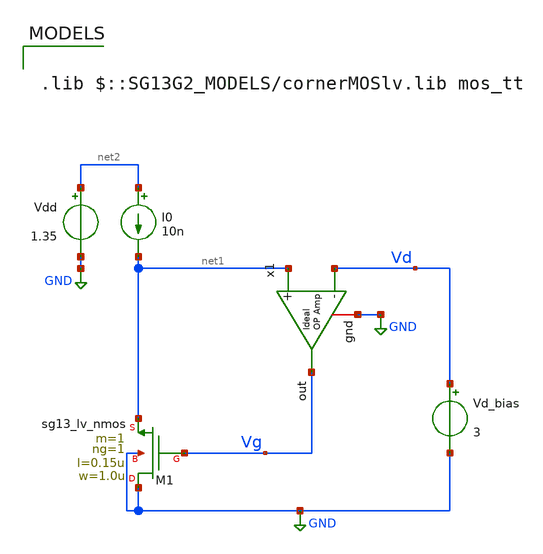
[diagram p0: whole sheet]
** sch_path: ihp_tutorials/nmos_ext_sigma_v2.sch
**.subckt nmos_ext_sigma_v2
x1 Vg net1 Vd GND ampOp_ideal
I0 net2 net1 10n
Vd_bias Vd GND 3
Vdd net2 GND 1.35
XM1 GND Vg net1 GND sg13_lv_nmos w=1.0u l=0.15u ng=1 m=1 mm_ok=1
**** begin user architecture code



.control
pre_osdi ./psp103_nqs.osdi
save all

dc Vd_bias  0.1 1.6 25.9m

let vd_interp = 1.35/3
let sigma = -deriv(V(vg))/deriv(V(vd))
save sigma

echo
echo
echo


echo Sigma @ VD=$&vd_interp:
meas dc sigma_value FIND sigma WHEN V(vd)=vd_interp

echo
echo
echo
write nmos_ext_sigma_v2.raw

.endc





.lib $::SG13G2_MODELS/cornerMOSlv.lib mos_tt

**** end user architecture code
**.ends

* expanding   symbol:  /home/gmaranhao/Desktop/gf180_work/auxLib/ampOp_ideal.sym # of pins=4
** sym_path: gf_tutorials/auxLib/ampOp_ideal.sym
** sch_path: gf_tutorials/auxLib/ampOp_ideal.sch
.subckt ampOp_ideal out + - gnd
*.ipin +
*.ipin -
*.opin out
*.iopin gnd
E1 out gnd + - 10000000
.ends

.GLOBAL GND
.end
